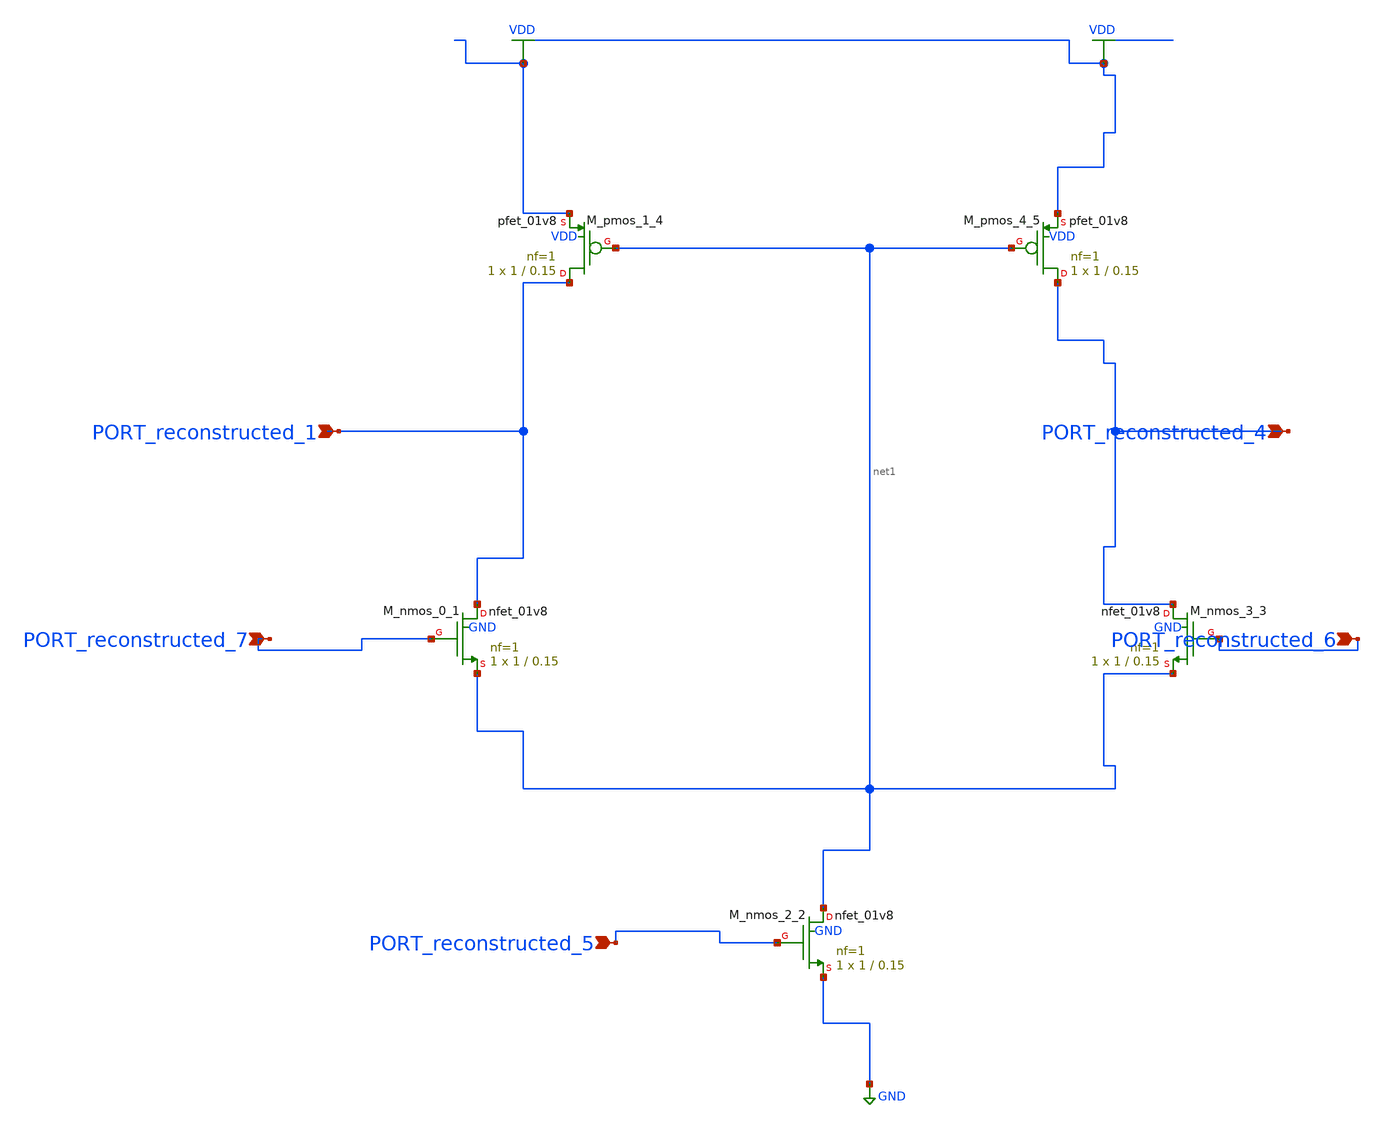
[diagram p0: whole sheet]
** sch_path: schematics/AMSNet/250.sch
**.subckt 250 PORT_reconstructed_5 PORT_reconstructed_6 PORT_reconstructed_7 PORT_reconstructed_4
*+ PORT_reconstructed_1
*.ipin PORT_reconstructed_5
*.ipin PORT_reconstructed_6
*.ipin PORT_reconstructed_7
*.ipin PORT_reconstructed_4
*.ipin PORT_reconstructed_1
XM_nmos_0_1 PORT_reconstructed_1 PORT_reconstructed_7 net1 GND sky130_fd_pr__nfet_01v8 L=0.15 W=1 nf=1
+ ad='int((1 + 1)/2) * 1 / 1 * 0.29' as='int((1 + 2)/2) * 1 / 1 * 0.29' pd='2*int((1 + 1)/2) * (1 / 1 + 0.29)'
+ ps='2*int((1 + 2)/2) * (1 / 1 + 0.29)' nrd='0.29 / 1 ' nrs='0.29 / 1 ' sa=0 sb=0 sd=0 mult=1 m=1
XM_nmos_2_2 net1 PORT_reconstructed_5 GND GND sky130_fd_pr__nfet_01v8 L=0.15 W=1 nf=1 ad='int((1 + 1)/2) * 1 / 1 * 0.29'
+ as='int((1 + 2)/2) * 1 / 1 * 0.29' pd='2*int((1 + 1)/2) * (1 / 1 + 0.29)' ps='2*int((1 + 2)/2) * (1 / 1 + 0.29)'
+ nrd='0.29 / 1 ' nrs='0.29 / 1 ' sa=0 sb=0 sd=0 mult=1 m=1
XM_nmos_3_3 PORT_reconstructed_4 PORT_reconstructed_6 net1 GND sky130_fd_pr__nfet_01v8 L=0.15 W=1 nf=1
+ ad='int((1 + 1)/2) * 1 / 1 * 0.29' as='int((1 + 2)/2) * 1 / 1 * 0.29' pd='2*int((1 + 1)/2) * (1 / 1 + 0.29)'
+ ps='2*int((1 + 2)/2) * (1 / 1 + 0.29)' nrd='0.29 / 1 ' nrs='0.29 / 1 ' sa=0 sb=0 sd=0 mult=1 m=1
XM_pmos_1_4 PORT_reconstructed_1 net1 VDD VDD sky130_fd_pr__pfet_01v8 L=0.15 W=1 nf=1 ad='int((1 + 1)/2) * 1 / 1 * 0.29'
+ as='int((1 + 2)/2) * 1 / 1 * 0.29' pd='2*int((1 + 1)/2) * (1 / 1 + 0.29)' ps='2*int((1 + 2)/2) * (1 / 1 + 0.29)'
+ nrd='0.29 / 1 ' nrs='0.29 / 1 ' sa=0 sb=0 sd=0 mult=1 m=1
XM_pmos_4_5 PORT_reconstructed_4 net1 VDD VDD sky130_fd_pr__pfet_01v8 L=0.15 W=1 nf=1 ad='int((1 + 1)/2) * 1 / 1 * 0.29'
+ as='int((1 + 2)/2) * 1 / 1 * 0.29' pd='2*int((1 + 1)/2) * (1 / 1 + 0.29)' ps='2*int((1 + 2)/2) * (1 / 1 + 0.29)'
+ nrd='0.29 / 1 ' nrs='0.29 / 1 ' sa=0 sb=0 sd=0 mult=1 m=1
**.ends
.GLOBAL GND
.GLOBAL VDD
.end
